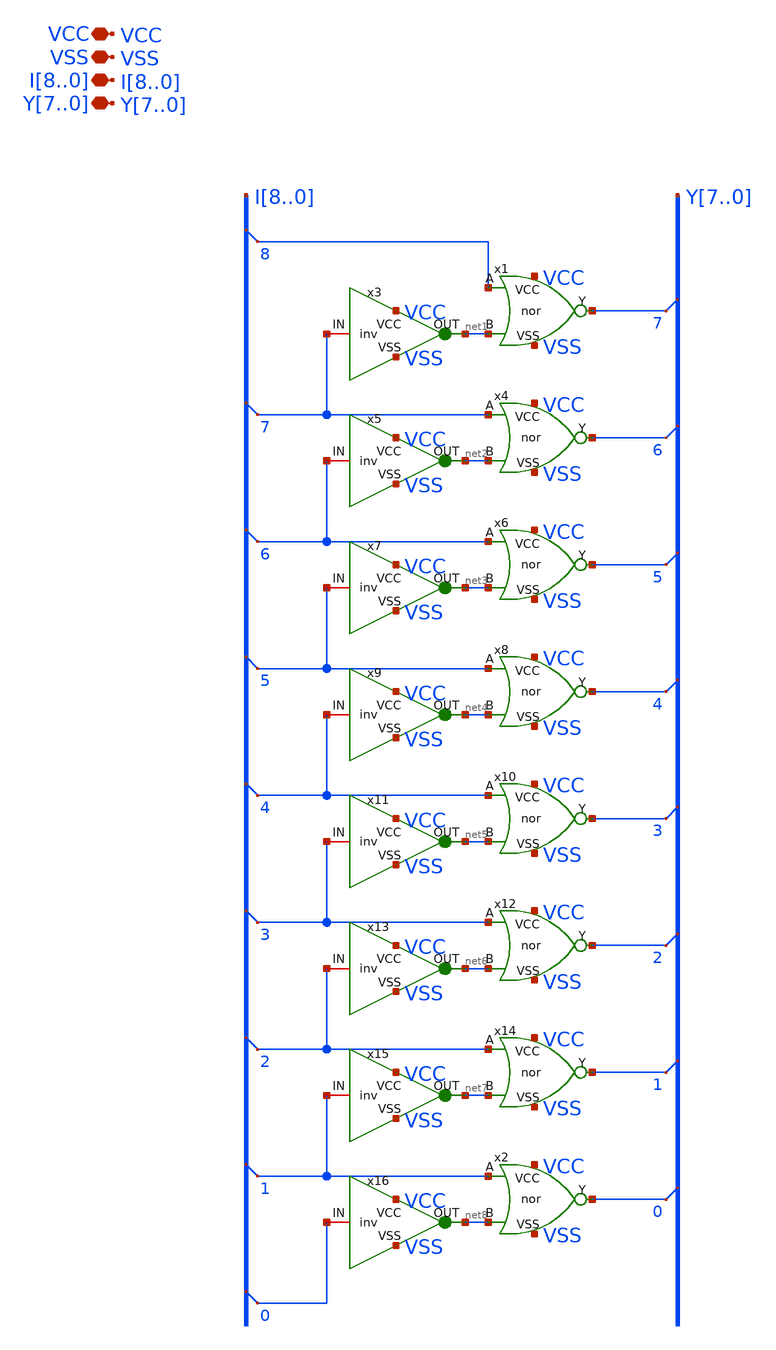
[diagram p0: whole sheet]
** sch_path: peripherals/priority_selector.sch
**.subckt priority_selector I8,I7,I6,I5,I4,I3,I2,I1,I0 Y7,Y6,Y5,Y4,Y3,Y2,Y1,Y0 VSS VCC
*.iopin I8,I7,I6,I5,I4,I3,I2,I1,I0
*.iopin Y7,Y6,Y5,Y4,Y3,Y2,Y1,Y0
*.iopin VSS
*.iopin VCC
x1 VCC Y7 I8 net1 VSS nor
* tap: I[8..0] --> I8
* tap: I[8..0] --> I7
x3 VCC I7 net1 VSS inv
x4 VCC Y6 I7 net2 VSS nor
x5 VCC I6 net2 VSS inv
* tap: I[8..0] --> I6
x6 VCC Y5 I6 net3 VSS nor
x7 VCC I5 net3 VSS inv
* tap: I[8..0] --> I5
x8 VCC Y4 I5 net4 VSS nor
x9 VCC I4 net4 VSS inv
* tap: I[8..0] --> I4
x10 VCC Y3 I4 net5 VSS nor
x11 VCC I3 net5 VSS inv
* tap: I[8..0] --> I3
x12 VCC Y2 I3 net6 VSS nor
x13 VCC I2 net6 VSS inv
* tap: I[8..0] --> I2
x14 VCC Y1 I2 net7 VSS nor
x15 VCC I1 net7 VSS inv
* tap: I[8..0] --> I1
* tap: Y[7..0] --> Y7
* tap: Y[7..0] --> Y6
* tap: Y[7..0] --> Y5
* tap: Y[7..0] --> Y4
* tap: Y[7..0] --> Y3
* tap: Y[7..0] --> Y2
* tap: Y[7..0] --> Y1
x2 VCC Y0 I1 net8 VSS nor
x16 VCC I0 net8 VSS inv
* tap: I[8..0] --> I0
* tap: Y[7..0] --> Y0
**.ends

* expanding   symbol:  logic gates/nor.sym # of pins=5
** sym_path: logic gates/nor.sym
** sch_path: logic gates/nor.sch
.subckt nor VCC Y A B VSS
*.iopin VCC
*.iopin VSS
*.iopin Y
*.iopin A
*.iopin B
XM2 Y B VSS VSS sky130_fd_pr__nfet_01v8 L=0.15 W=1 nf=1 ad='int((1 + 1)/2) * 1 / 1 * 0.29' as='int((1 + 2)/2) * 1 / 1 * 0.29'
+ pd='2*int((1 + 1)/2) * (1 / 1 + 0.29)' ps='2*int((1 + 2)/2) * (1 / 1 + 0.29)' nrd='0.29 / 1 ' nrs='0.29 / 1 '
+ sa=0 sb=0 sd=0 mult=1 m=1
XM11 Y B net1 VCC sky130_fd_pr__pfet_01v8 L=0.15 W=1 nf=1 ad='int((nf+1)/2) * W/nf * 0.29' as='int((nf+2)/2) * W/nf * 0.29'
+ pd='2*int((nf+1)/2) * (W/nf + 0.29)' ps='2*int((nf+2)/2) * (W/nf + 0.29)' nrd='0.29 / W' nrs='0.29 / W'
+ sa=0 sb=0 sd=0 mult=1 m=1
XM1 Y A VSS VSS sky130_fd_pr__nfet_01v8 L=0.15 W=1 nf=1 ad='int((1 + 1)/2) * 1 / 1 * 0.29' as='int((1 + 2)/2) * 1 / 1 * 0.29'
+ pd='2*int((1 + 1)/2) * (1 / 1 + 0.29)' ps='2*int((1 + 2)/2) * (1 / 1 + 0.29)' nrd='0.29 / 1 ' nrs='0.29 / 1 '
+ sa=0 sb=0 sd=0 mult=1 m=1
XM3 net1 A VCC VCC sky130_fd_pr__pfet_01v8 L=0.15 W=1 nf=1 ad='int((nf+1)/2) * W/nf * 0.29' as='int((nf+2)/2) * W/nf * 0.29'
+ pd='2*int((nf+1)/2) * (W/nf + 0.29)' ps='2*int((nf+2)/2) * (W/nf + 0.29)' nrd='0.29 / W' nrs='0.29 / W'
+ sa=0 sb=0 sd=0 mult=1 m=1
.ends


* expanding   symbol:  inv.sym # of pins=4
** sym_path: peripherals/inv.sym
** sch_path: peripherals/inv.sch
.subckt inv VCC IN OUT VSS
*.iopin VCC
*.iopin IN
*.iopin OUT
*.iopin VSS
XM1 OUT IN VSS VSS sky130_fd_pr__nfet_01v8 L=0.15 W=0.5 nf=1 ad='int((nf+1)/2) * W/nf * 0.29' as='int((nf+2)/2) * W/nf * 0.29'
+ pd='2*int((nf+1)/2) * (W/nf + 0.29)' ps='2*int((nf+2)/2) * (W/nf + 0.29)' nrd='0.29 / W' nrs='0.29 / W'
+ sa=0 sb=0 sd=0 mult=1 m=1
XM2 OUT IN VCC VCC sky130_fd_pr__pfet_01v8 L=0.15 W=1.05 nf=1 ad='int((nf+1)/2) * W/nf * 0.29' as='int((nf+2)/2) * W/nf * 0.29'
+ pd='2*int((nf+1)/2) * (W/nf + 0.29)' ps='2*int((nf+2)/2) * (W/nf + 0.29)' nrd='0.29 / W' nrs='0.29 / W'
+ sa=0 sb=0 sd=0 mult=1 m=1
.ends

.end
